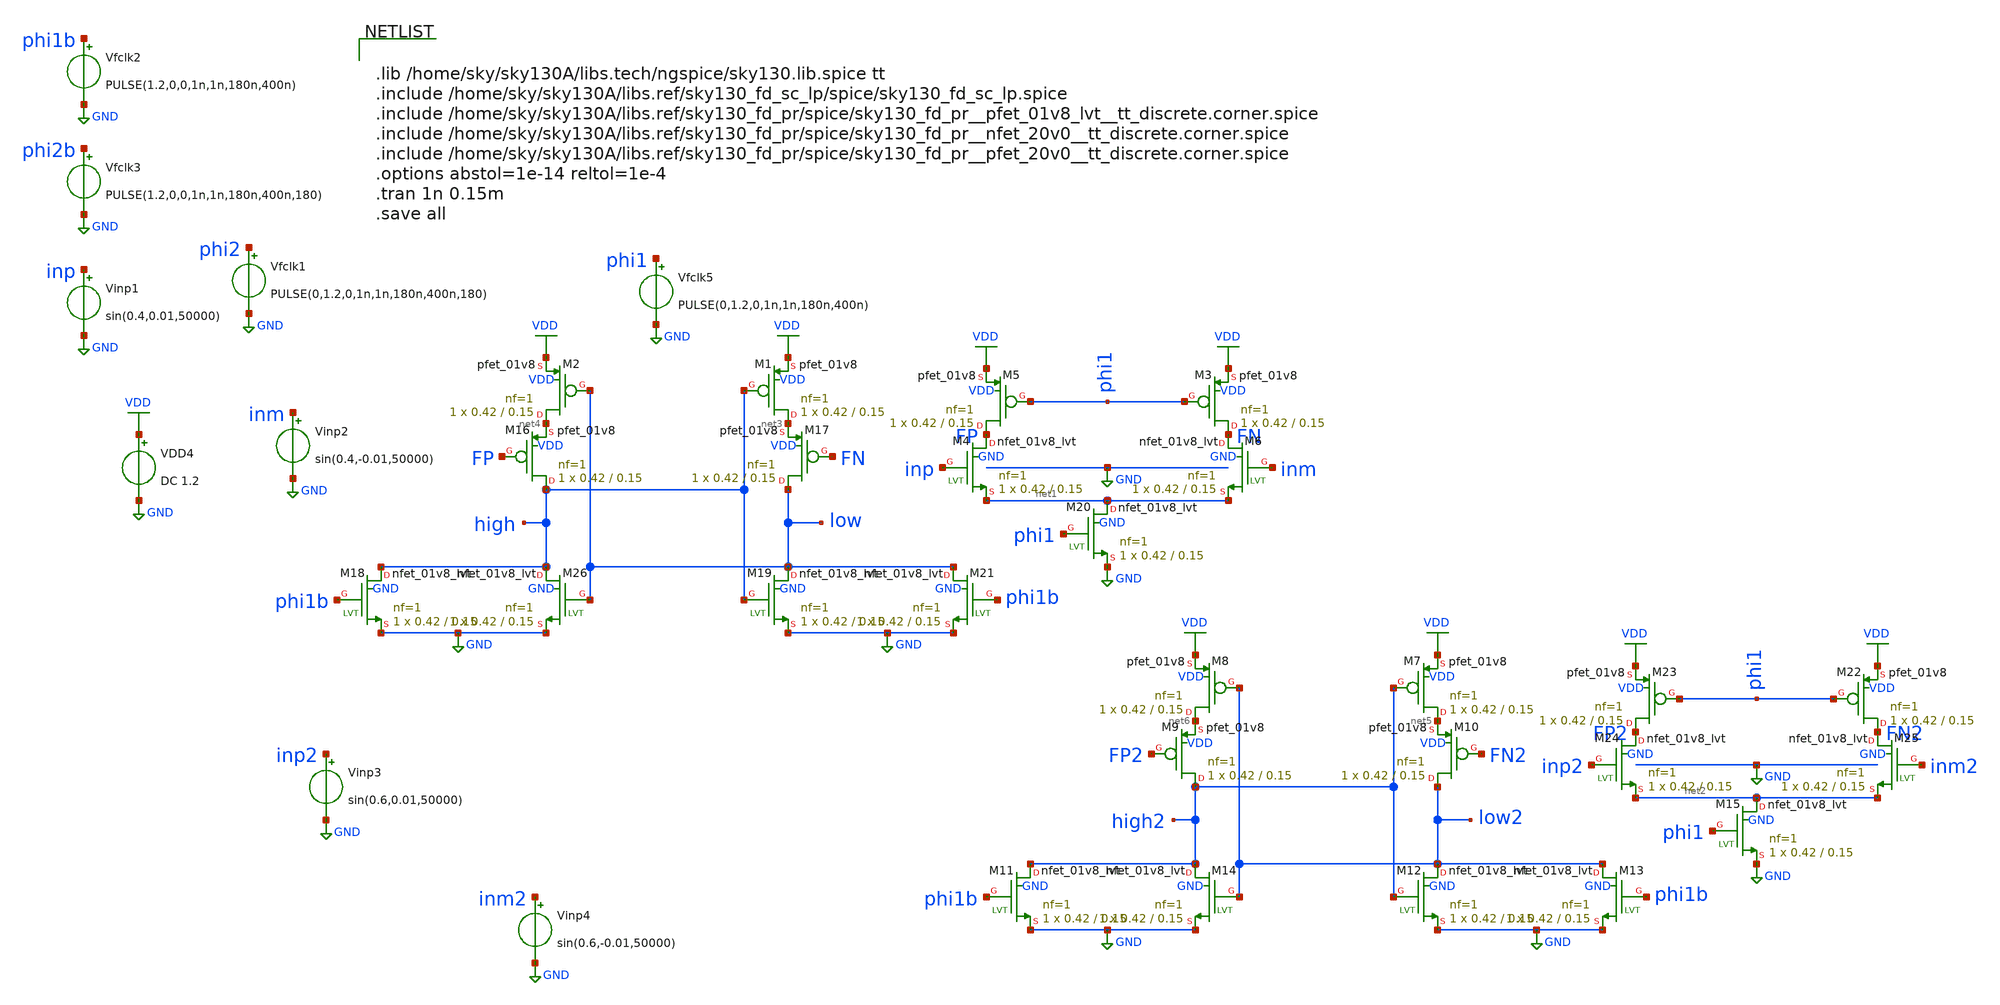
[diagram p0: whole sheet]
** sch_path: xschem/tryandtest/archive/comparator_AZ_tb.sch
**.subckt comparator_AZ_tb
VDD4 VDD GND DC 1.2
Vfclk5 phi1 GND PULSE(0,1.2,0,1n,1n,180n,400n)
XM1 net3 high VDD VDD sky130_fd_pr__pfet_01v8 L=0.15 W=0.42 nf=1 ad='int((nf+1)/2) * W/nf * 0.29' as='int((nf+2)/2) * W/nf * 0.29'
+ pd='2*int((nf+1)/2) * (W/nf + 0.29)' ps='2*int((nf+2)/2) * (W/nf + 0.29)' nrd='0.29 / W' nrs='0.29 / W'
+ sa=0 sb=0 sd=0 mult=1 m=1
XM2 net4 low VDD VDD sky130_fd_pr__pfet_01v8 L=0.15 W=0.42 nf=1 ad='int((nf+1)/2) * W/nf * 0.29' as='int((nf+2)/2) * W/nf * 0.29'
+ pd='2*int((nf+1)/2) * (W/nf + 0.29)' ps='2*int((nf+2)/2) * (W/nf + 0.29)' nrd='0.29 / W' nrs='0.29 / W'
+ sa=0 sb=0 sd=0 mult=1 m=1
XM16 high FP net4 VDD sky130_fd_pr__pfet_01v8 L=0.15 W=0.42 nf=1 ad='int((nf+1)/2) * W/nf * 0.29' as='int((nf+2)/2) * W/nf * 0.29'
+ pd='2*int((nf+1)/2) * (W/nf + 0.29)' ps='2*int((nf+2)/2) * (W/nf + 0.29)' nrd='0.29 / W' nrs='0.29 / W'
+ sa=0 sb=0 sd=0 mult=1 m=1
XM17 low FN net3 VDD sky130_fd_pr__pfet_01v8 L=0.15 W=0.42 nf=1 ad='int((nf+1)/2) * W/nf * 0.29' as='int((nf+2)/2) * W/nf * 0.29'
+ pd='2*int((nf+1)/2) * (W/nf + 0.29)' ps='2*int((nf+2)/2) * (W/nf + 0.29)' nrd='0.29 / W' nrs='0.29 / W'
+ sa=0 sb=0 sd=0 mult=1 m=1
Vinp1 inp GND sin(0.4,0.01,50000)
Vinp2 inm GND sin(0.4,-0.01,50000)
Vfclk1 phi2 GND PULSE(0,1.2,0,1n,1n,180n,400n,180)
Vfclk2 phi1b GND PULSE(1.2,0,0,1n,1n,180n,400n)
Vfclk3 phi2b GND PULSE(1.2,0,0,1n,1n,180n,400n,180)
XM3 FN phi1 VDD VDD sky130_fd_pr__pfet_01v8 L=0.15 W=0.42 nf=1 ad='int((nf+1)/2) * W/nf * 0.29' as='int((nf+2)/2) * W/nf * 0.29'
+ pd='2*int((nf+1)/2) * (W/nf + 0.29)' ps='2*int((nf+2)/2) * (W/nf + 0.29)' nrd='0.29 / W' nrs='0.29 / W'
+ sa=0 sb=0 sd=0 mult=1 m=1
XM5 FP phi1 VDD VDD sky130_fd_pr__pfet_01v8 L=0.15 W=0.42 nf=1 ad='int((nf+1)/2) * W/nf * 0.29' as='int((nf+2)/2) * W/nf * 0.29'
+ pd='2*int((nf+1)/2) * (W/nf + 0.29)' ps='2*int((nf+2)/2) * (W/nf + 0.29)' nrd='0.29 / W' nrs='0.29 / W'
+ sa=0 sb=0 sd=0 mult=1 m=1
XM4 FP inp net1 GND sky130_fd_pr__nfet_01v8_lvt L=0.15 W=0.42 nf=1 ad='int((nf+1)/2) * W/nf * 0.29' as='int((nf+2)/2) * W/nf * 0.29'
+ pd='2*int((nf+1)/2) * (W/nf + 0.29)' ps='2*int((nf+2)/2) * (W/nf + 0.29)' nrd='0.29 / W' nrs='0.29 / W'
+ sa=0 sb=0 sd=0 mult=1 m=1
XM6 FN inm net1 GND sky130_fd_pr__nfet_01v8_lvt L=0.15 W=0.42 nf=1 ad='int((nf+1)/2) * W/nf * 0.29' as='int((nf+2)/2) * W/nf * 0.29'
+ pd='2*int((nf+1)/2) * (W/nf + 0.29)' ps='2*int((nf+2)/2) * (W/nf + 0.29)' nrd='0.29 / W' nrs='0.29 / W'
+ sa=0 sb=0 sd=0 mult=1 m=1
XM7 net5 high2 VDD VDD sky130_fd_pr__pfet_01v8 L=0.15 W=0.42 nf=1 ad='int((nf+1)/2) * W/nf * 0.29' as='int((nf+2)/2) * W/nf * 0.29'
+ pd='2*int((nf+1)/2) * (W/nf + 0.29)' ps='2*int((nf+2)/2) * (W/nf + 0.29)' nrd='0.29 / W' nrs='0.29 / W'
+ sa=0 sb=0 sd=0 mult=1 m=1
XM8 net6 low2 VDD VDD sky130_fd_pr__pfet_01v8 L=0.15 W=0.42 nf=1 ad='int((nf+1)/2) * W/nf * 0.29' as='int((nf+2)/2) * W/nf * 0.29'
+ pd='2*int((nf+1)/2) * (W/nf + 0.29)' ps='2*int((nf+2)/2) * (W/nf + 0.29)' nrd='0.29 / W' nrs='0.29 / W'
+ sa=0 sb=0 sd=0 mult=1 m=1
XM9 high2 FP2 net6 VDD sky130_fd_pr__pfet_01v8 L=0.15 W=0.42 nf=1 ad='int((nf+1)/2) * W/nf * 0.29' as='int((nf+2)/2) * W/nf * 0.29'
+ pd='2*int((nf+1)/2) * (W/nf + 0.29)' ps='2*int((nf+2)/2) * (W/nf + 0.29)' nrd='0.29 / W' nrs='0.29 / W'
+ sa=0 sb=0 sd=0 mult=1 m=1
XM10 low2 FN2 net5 VDD sky130_fd_pr__pfet_01v8 L=0.15 W=0.42 nf=1 ad='int((nf+1)/2) * W/nf * 0.29' as='int((nf+2)/2) * W/nf * 0.29'
+ pd='2*int((nf+1)/2) * (W/nf + 0.29)' ps='2*int((nf+2)/2) * (W/nf + 0.29)' nrd='0.29 / W' nrs='0.29 / W'
+ sa=0 sb=0 sd=0 mult=1 m=1
XM22 FN2 phi1 VDD VDD sky130_fd_pr__pfet_01v8 L=0.15 W=0.42 nf=1 ad='int((nf+1)/2) * W/nf * 0.29' as='int((nf+2)/2) * W/nf * 0.29'
+ pd='2*int((nf+1)/2) * (W/nf + 0.29)' ps='2*int((nf+2)/2) * (W/nf + 0.29)' nrd='0.29 / W' nrs='0.29 / W'
+ sa=0 sb=0 sd=0 mult=1 m=1
XM23 FP2 phi1 VDD VDD sky130_fd_pr__pfet_01v8 L=0.15 W=0.42 nf=1 ad='int((nf+1)/2) * W/nf * 0.29' as='int((nf+2)/2) * W/nf * 0.29'
+ pd='2*int((nf+1)/2) * (W/nf + 0.29)' ps='2*int((nf+2)/2) * (W/nf + 0.29)' nrd='0.29 / W' nrs='0.29 / W'
+ sa=0 sb=0 sd=0 mult=1 m=1
XM24 FP2 inp2 net2 GND sky130_fd_pr__nfet_01v8_lvt L=0.15 W=0.42 nf=1 ad='int((nf+1)/2) * W/nf * 0.29'
+ as='int((nf+2)/2) * W/nf * 0.29' pd='2*int((nf+1)/2) * (W/nf + 0.29)' ps='2*int((nf+2)/2) * (W/nf + 0.29)'
+ nrd='0.29 / W' nrs='0.29 / W' sa=0 sb=0 sd=0 mult=1 m=1
XM25 FN2 inm2 net2 GND sky130_fd_pr__nfet_01v8_lvt L=0.15 W=0.42 nf=1 ad='int((nf+1)/2) * W/nf * 0.29'
+ as='int((nf+2)/2) * W/nf * 0.29' pd='2*int((nf+1)/2) * (W/nf + 0.29)' ps='2*int((nf+2)/2) * (W/nf + 0.29)'
+ nrd='0.29 / W' nrs='0.29 / W' sa=0 sb=0 sd=0 mult=1 m=1
Vinp3 inp2 GND sin(0.6,0.01,50000)
Vinp4 inm2 GND sin(0.6,-0.01,50000)
XM11 high2 phi1b GND GND sky130_fd_pr__nfet_01v8_lvt L=0.15 W=0.42 nf=1 ad='int((nf+1)/2) * W/nf * 0.29'
+ as='int((nf+2)/2) * W/nf * 0.29' pd='2*int((nf+1)/2) * (W/nf + 0.29)' ps='2*int((nf+2)/2) * (W/nf + 0.29)'
+ nrd='0.29 / W' nrs='0.29 / W' sa=0 sb=0 sd=0 mult=1 m=1
XM12 low2 high2 GND GND sky130_fd_pr__nfet_01v8_lvt L=0.15 W=0.42 nf=1 ad='int((nf+1)/2) * W/nf * 0.29'
+ as='int((nf+2)/2) * W/nf * 0.29' pd='2*int((nf+1)/2) * (W/nf + 0.29)' ps='2*int((nf+2)/2) * (W/nf + 0.29)'
+ nrd='0.29 / W' nrs='0.29 / W' sa=0 sb=0 sd=0 mult=1 m=1
XM13 low2 phi1b GND GND sky130_fd_pr__nfet_01v8_lvt L=0.15 W=0.42 nf=1 ad='int((nf+1)/2) * W/nf * 0.29'
+ as='int((nf+2)/2) * W/nf * 0.29' pd='2*int((nf+1)/2) * (W/nf + 0.29)' ps='2*int((nf+2)/2) * (W/nf + 0.29)'
+ nrd='0.29 / W' nrs='0.29 / W' sa=0 sb=0 sd=0 mult=1 m=1
XM14 high2 low2 GND GND sky130_fd_pr__nfet_01v8_lvt L=0.15 W=0.42 nf=1 ad='int((nf+1)/2) * W/nf * 0.29'
+ as='int((nf+2)/2) * W/nf * 0.29' pd='2*int((nf+1)/2) * (W/nf + 0.29)' ps='2*int((nf+2)/2) * (W/nf + 0.29)'
+ nrd='0.29 / W' nrs='0.29 / W' sa=0 sb=0 sd=0 mult=1 m=1
XM15 net2 phi1 GND GND sky130_fd_pr__nfet_01v8_lvt L=0.15 W=0.42 nf=1 ad='int((nf+1)/2) * W/nf * 0.29'
+ as='int((nf+2)/2) * W/nf * 0.29' pd='2*int((nf+1)/2) * (W/nf + 0.29)' ps='2*int((nf+2)/2) * (W/nf + 0.29)'
+ nrd='0.29 / W' nrs='0.29 / W' sa=0 sb=0 sd=0 mult=1 m=1
XM18 high phi1b GND GND sky130_fd_pr__nfet_01v8_lvt L=0.15 W=0.42 nf=1 ad='int((nf+1)/2) * W/nf * 0.29'
+ as='int((nf+2)/2) * W/nf * 0.29' pd='2*int((nf+1)/2) * (W/nf + 0.29)' ps='2*int((nf+2)/2) * (W/nf + 0.29)'
+ nrd='0.29 / W' nrs='0.29 / W' sa=0 sb=0 sd=0 mult=1 m=1
XM19 low high GND GND sky130_fd_pr__nfet_01v8_lvt L=0.15 W=0.42 nf=1 ad='int((nf+1)/2) * W/nf * 0.29'
+ as='int((nf+2)/2) * W/nf * 0.29' pd='2*int((nf+1)/2) * (W/nf + 0.29)' ps='2*int((nf+2)/2) * (W/nf + 0.29)'
+ nrd='0.29 / W' nrs='0.29 / W' sa=0 sb=0 sd=0 mult=1 m=1
XM20 net1 phi1 GND GND sky130_fd_pr__nfet_01v8_lvt L=0.15 W=0.42 nf=1 ad='int((nf+1)/2) * W/nf * 0.29'
+ as='int((nf+2)/2) * W/nf * 0.29' pd='2*int((nf+1)/2) * (W/nf + 0.29)' ps='2*int((nf+2)/2) * (W/nf + 0.29)'
+ nrd='0.29 / W' nrs='0.29 / W' sa=0 sb=0 sd=0 mult=1 m=1
XM21 low phi1b GND GND sky130_fd_pr__nfet_01v8_lvt L=0.15 W=0.42 nf=1 ad='int((nf+1)/2) * W/nf * 0.29'
+ as='int((nf+2)/2) * W/nf * 0.29' pd='2*int((nf+1)/2) * (W/nf + 0.29)' ps='2*int((nf+2)/2) * (W/nf + 0.29)'
+ nrd='0.29 / W' nrs='0.29 / W' sa=0 sb=0 sd=0 mult=1 m=1
XM26 high low GND GND sky130_fd_pr__nfet_01v8_lvt L=0.15 W=0.42 nf=1 ad='int((nf+1)/2) * W/nf * 0.29'
+ as='int((nf+2)/2) * W/nf * 0.29' pd='2*int((nf+1)/2) * (W/nf + 0.29)' ps='2*int((nf+2)/2) * (W/nf + 0.29)'
+ nrd='0.29 / W' nrs='0.29 / W' sa=0 sb=0 sd=0 mult=1 m=1
**** begin user architecture code


.lib /home/sky/sky130A/libs.tech/ngspice/sky130.lib.spice tt
.include /home/sky/sky130A/libs.ref/sky130_fd_sc_lp/spice/sky130_fd_sc_lp.spice
.include /home/sky/sky130A/libs.ref/sky130_fd_pr/spice/sky130_fd_pr__pfet_01v8_lvt__tt_discrete.corner.spice
.include /home/sky/sky130A/libs.ref/sky130_fd_pr/spice/sky130_fd_pr__nfet_20v0__tt_discrete.corner.spice
.include /home/sky/sky130A/libs.ref/sky130_fd_pr/spice/sky130_fd_pr__pfet_20v0__tt_discrete.corner.spice
.options abstol=1e-14 reltol=1e-4
.tran 1n 0.15m
.save all


**** end user architecture code
**.ends
.GLOBAL GND
.GLOBAL VDD
.end
